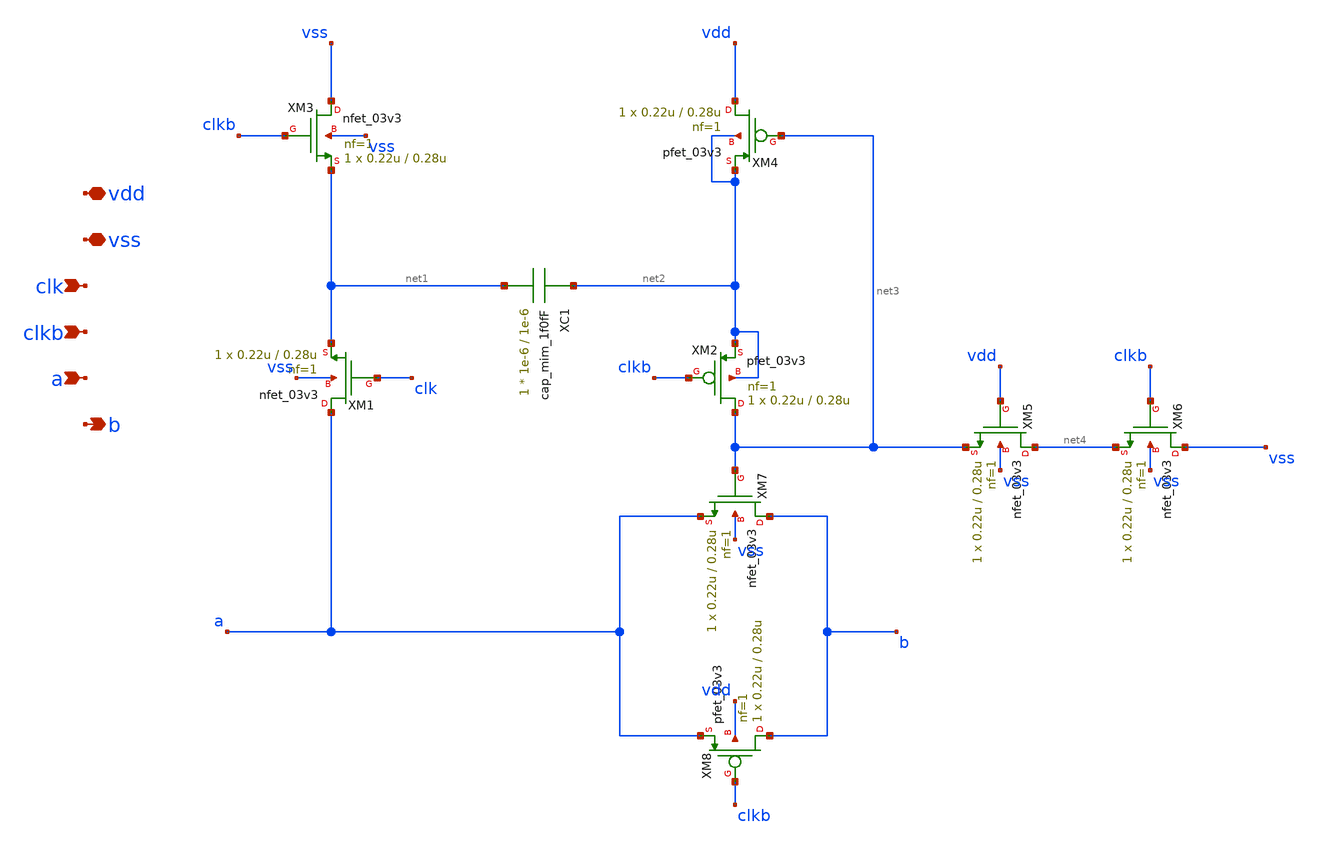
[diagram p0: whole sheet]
** sch_path: designs/libs/sample_and_hold/sample_and_hold.sch
**.subckt sample_and_hold vdd vss clk clkb a b
*.iopin vdd
*.iopin vss
*.ipin clk
*.ipin clkb
*.ipin a
*.opin b
XM1 a clk net1 vss nfet_03v3 L=0.28u W=0.22u nf=1 ad='int((nf+1)/2) * W/nf * 0.18u' as='int((nf+2)/2) * W/nf * 0.18u'
+ pd='2*int((nf+1)/2) * (W/nf + 0.18u)' ps='2*int((nf+2)/2) * (W/nf + 0.18u)' nrd='0.18u / W' nrs='0.18u / W'
+ sa=0 sb=0 sd=0 m=1
XM2 net3 clkb net2 net2 pfet_03v3 L=0.28u W=0.22u nf=1 ad='int((nf+1)/2) * W/nf * 0.18u' as='int((nf+2)/2) * W/nf * 0.18u'
+ pd='2*int((nf+1)/2) * (W/nf + 0.18u)' ps='2*int((nf+2)/2) * (W/nf + 0.18u)' nrd='0.18u / W' nrs='0.18u / W'
+ sa=0 sb=0 sd=0 m=1
XM3 vss clkb net1 vss nfet_03v3 L=0.28u W=0.22u nf=1 ad='int((nf+1)/2) * W/nf * 0.18u' as='int((nf+2)/2) * W/nf * 0.18u'
+ pd='2*int((nf+1)/2) * (W/nf + 0.18u)' ps='2*int((nf+2)/2) * (W/nf + 0.18u)' nrd='0.18u / W' nrs='0.18u / W'
+ sa=0 sb=0 sd=0 m=1
XM4 vdd net3 net2 net2 pfet_03v3 L=0.28u W=0.22u nf=1 ad='int((nf+1)/2) * W/nf * 0.18u' as='int((nf+2)/2) * W/nf * 0.18u'
+ pd='2*int((nf+1)/2) * (W/nf + 0.18u)' ps='2*int((nf+2)/2) * (W/nf + 0.18u)' nrd='0.18u / W' nrs='0.18u / W'
+ sa=0 sb=0 sd=0 m=1
XM5 net4 vdd net3 vss nfet_03v3 L=0.28u W=0.22u nf=1 ad='int((nf+1)/2) * W/nf * 0.18u' as='int((nf+2)/2) * W/nf * 0.18u'
+ pd='2*int((nf+1)/2) * (W/nf + 0.18u)' ps='2*int((nf+2)/2) * (W/nf + 0.18u)' nrd='0.18u / W' nrs='0.18u / W'
+ sa=0 sb=0 sd=0 m=1
XM6 vss clkb net4 vss nfet_03v3 L=0.28u W=0.22u nf=1 ad='int((nf+1)/2) * W/nf * 0.18u' as='int((nf+2)/2) * W/nf * 0.18u'
+ pd='2*int((nf+1)/2) * (W/nf + 0.18u)' ps='2*int((nf+2)/2) * (W/nf + 0.18u)' nrd='0.18u / W' nrs='0.18u / W'
+ sa=0 sb=0 sd=0 m=1
XM7 b net3 a vss nfet_03v3 L=0.28u W=0.22u nf=1 ad='int((nf+1)/2) * W/nf * 0.18u' as='int((nf+2)/2) * W/nf * 0.18u'
+ pd='2*int((nf+1)/2) * (W/nf + 0.18u)' ps='2*int((nf+2)/2) * (W/nf + 0.18u)' nrd='0.18u / W' nrs='0.18u / W'
+ sa=0 sb=0 sd=0 m=1
XM8 b clkb a vdd pfet_03v3 L=0.28u W=0.22u nf=1 ad='int((nf+1)/2) * W/nf * 0.18u' as='int((nf+2)/2) * W/nf * 0.18u'
+ pd='2*int((nf+1)/2) * (W/nf + 0.18u)' ps='2*int((nf+2)/2) * (W/nf + 0.18u)' nrd='0.18u / W' nrs='0.18u / W'
+ sa=0 sb=0 sd=0 m=1
XC1 net2 net1 cap_mim_1f0fF c_width=1e-6 c_length=1e-6 m=1
**.ends
.end
